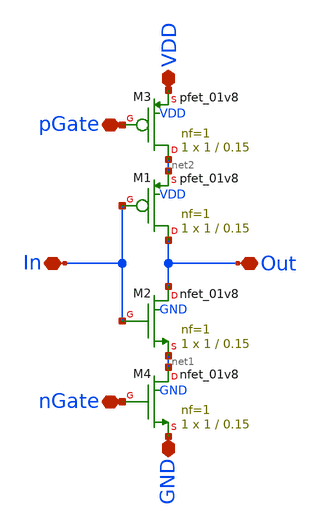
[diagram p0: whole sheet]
** sch_path: VCO_circuit/current_mirror.sch
**.subckt current_mirror Out In VDD GND pGate nGate
*.iopin Out
*.iopin In
*.iopin VDD
*.iopin GND
*.iopin pGate
*.iopin nGate
XM1 Out In net2 VDD sky130_fd_pr__pfet_01v8 L=0.15 W=1 nf=1 ad='int((nf+1)/2) * W/nf * 0.29' as='int((nf+2)/2) * W/nf * 0.29'
+ pd='2*int((nf+1)/2) * (W/nf + 0.29)' ps='2*int((nf+2)/2) * (W/nf + 0.29)' nrd='0.29 / W' nrs='0.29 / W'
+ sa=0 sb=0 sd=0 mult=1 m=1
XM2 Out In net1 GND sky130_fd_pr__nfet_01v8 L=0.15 W=1 nf=1 ad='int((nf+1)/2) * W/nf * 0.29' as='int((nf+2)/2) * W/nf * 0.29'
+ pd='2*int((nf+1)/2) * (W/nf + 0.29)' ps='2*int((nf+2)/2) * (W/nf + 0.29)' nrd='0.29 / W' nrs='0.29 / W'
+ sa=0 sb=0 sd=0 mult=1 m=1
XM3 net2 pGate VDD VDD sky130_fd_pr__pfet_01v8 L=0.15 W=1 nf=1 ad='int((nf+1)/2) * W/nf * 0.29' as='int((nf+2)/2) * W/nf * 0.29'
+ pd='2*int((nf+1)/2) * (W/nf + 0.29)' ps='2*int((nf+2)/2) * (W/nf + 0.29)' nrd='0.29 / W' nrs='0.29 / W'
+ sa=0 sb=0 sd=0 mult=1 m=1
XM4 net1 nGate GND GND sky130_fd_pr__nfet_01v8 L=0.15 W=1 nf=1 ad='int((nf+1)/2) * W/nf * 0.29' as='int((nf+2)/2) * W/nf * 0.29'
+ pd='2*int((nf+1)/2) * (W/nf + 0.29)' ps='2*int((nf+2)/2) * (W/nf + 0.29)' nrd='0.29 / W' nrs='0.29 / W'
+ sa=0 sb=0 sd=0 mult=1 m=1
**.ends
.end
